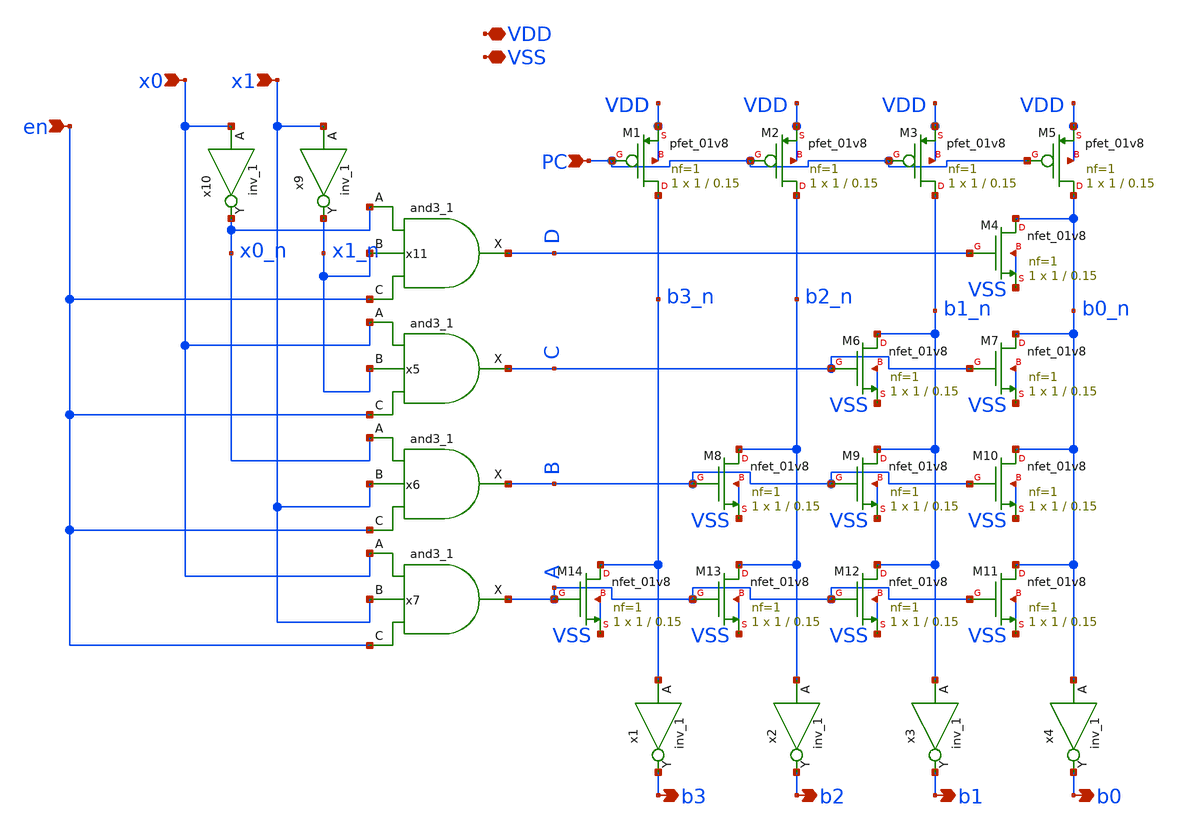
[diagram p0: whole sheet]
** sch_path: xschem/NOR_ROM_2bit.sch
**.subckt NOR_ROM_2bit VDD VSS x0 b3 x1 b2 b1 b0 PC en
*.iopin VDD
*.iopin VSS
*.ipin x0
*.opin b3
*.ipin x1
*.opin b2
*.opin b1
*.opin b0
*.ipin PC
*.ipin en
XM4 b0_n D VSS VSS sky130_fd_pr__nfet_01v8 L=0.15 W=1 nf=1 ad='int((nf+1)/2) * W/nf * 0.29' as='int((nf+2)/2) * W/nf * 0.29'
+ pd='2*int((nf+1)/2) * (W/nf + 0.29)' ps='2*int((nf+2)/2) * (W/nf + 0.29)' nrd='0.29 / W' nrs='0.29 / W'
+ sa=0 sb=0 sd=0 mult=1 m=1
XM6 b1_n C VSS VSS sky130_fd_pr__nfet_01v8 L=0.15 W=1 nf=1 ad='int((nf+1)/2) * W/nf * 0.29' as='int((nf+2)/2) * W/nf * 0.29'
+ pd='2*int((nf+1)/2) * (W/nf + 0.29)' ps='2*int((nf+2)/2) * (W/nf + 0.29)' nrd='0.29 / W' nrs='0.29 / W'
+ sa=0 sb=0 sd=0 mult=1 m=1
XM7 b0_n C VSS VSS sky130_fd_pr__nfet_01v8 L=0.15 W=1 nf=1 ad='int((nf+1)/2) * W/nf * 0.29' as='int((nf+2)/2) * W/nf * 0.29'
+ pd='2*int((nf+1)/2) * (W/nf + 0.29)' ps='2*int((nf+2)/2) * (W/nf + 0.29)' nrd='0.29 / W' nrs='0.29 / W'
+ sa=0 sb=0 sd=0 mult=1 m=1
XM8 b2_n B VSS VSS sky130_fd_pr__nfet_01v8 L=0.15 W=1 nf=1 ad='int((nf+1)/2) * W/nf * 0.29' as='int((nf+2)/2) * W/nf * 0.29'
+ pd='2*int((nf+1)/2) * (W/nf + 0.29)' ps='2*int((nf+2)/2) * (W/nf + 0.29)' nrd='0.29 / W' nrs='0.29 / W'
+ sa=0 sb=0 sd=0 mult=1 m=1
XM9 b1_n B VSS VSS sky130_fd_pr__nfet_01v8 L=0.15 W=1 nf=1 ad='int((nf+1)/2) * W/nf * 0.29' as='int((nf+2)/2) * W/nf * 0.29'
+ pd='2*int((nf+1)/2) * (W/nf + 0.29)' ps='2*int((nf+2)/2) * (W/nf + 0.29)' nrd='0.29 / W' nrs='0.29 / W'
+ sa=0 sb=0 sd=0 mult=1 m=1
XM10 b0_n B VSS VSS sky130_fd_pr__nfet_01v8 L=0.15 W=1 nf=1 ad='int((nf+1)/2) * W/nf * 0.29' as='int((nf+2)/2) * W/nf * 0.29'
+ pd='2*int((nf+1)/2) * (W/nf + 0.29)' ps='2*int((nf+2)/2) * (W/nf + 0.29)' nrd='0.29 / W' nrs='0.29 / W'
+ sa=0 sb=0 sd=0 mult=1 m=1
XM11 b0_n A VSS VSS sky130_fd_pr__nfet_01v8 L=0.15 W=1 nf=1 ad='int((nf+1)/2) * W/nf * 0.29' as='int((nf+2)/2) * W/nf * 0.29'
+ pd='2*int((nf+1)/2) * (W/nf + 0.29)' ps='2*int((nf+2)/2) * (W/nf + 0.29)' nrd='0.29 / W' nrs='0.29 / W'
+ sa=0 sb=0 sd=0 mult=1 m=1
XM12 b1_n A VSS VSS sky130_fd_pr__nfet_01v8 L=0.15 W=1 nf=1 ad='int((nf+1)/2) * W/nf * 0.29' as='int((nf+2)/2) * W/nf * 0.29'
+ pd='2*int((nf+1)/2) * (W/nf + 0.29)' ps='2*int((nf+2)/2) * (W/nf + 0.29)' nrd='0.29 / W' nrs='0.29 / W'
+ sa=0 sb=0 sd=0 mult=1 m=1
XM13 b2_n A VSS VSS sky130_fd_pr__nfet_01v8 L=0.15 W=1 nf=1 ad='int((nf+1)/2) * W/nf * 0.29' as='int((nf+2)/2) * W/nf * 0.29'
+ pd='2*int((nf+1)/2) * (W/nf + 0.29)' ps='2*int((nf+2)/2) * (W/nf + 0.29)' nrd='0.29 / W' nrs='0.29 / W'
+ sa=0 sb=0 sd=0 mult=1 m=1
XM14 b3_n A VSS VSS sky130_fd_pr__nfet_01v8 L=0.15 W=1 nf=1 ad='int((nf+1)/2) * W/nf * 0.29' as='int((nf+2)/2) * W/nf * 0.29'
+ pd='2*int((nf+1)/2) * (W/nf + 0.29)' ps='2*int((nf+2)/2) * (W/nf + 0.29)' nrd='0.29 / W' nrs='0.29 / W'
+ sa=0 sb=0 sd=0 mult=1 m=1
x1 b3_n VGND VNB VPB VPWR b3 sky130_fd_sc_hd__inv_1
x2 b2_n VGND VNB VPB VPWR b2 sky130_fd_sc_hd__inv_1
x3 b1_n VGND VNB VPB VPWR b1 sky130_fd_sc_hd__inv_1
x4 b0_n VGND VNB VPB VPWR b0 sky130_fd_sc_hd__inv_1
x9 x1 VGND VNB VPB VPWR x1_n sky130_fd_sc_hd__inv_1
x10 x0 VGND VNB VPB VPWR x0_n sky130_fd_sc_hd__inv_1
XM1 b3_n PC VDD VDD sky130_fd_pr__pfet_01v8 L=0.15 W=1 nf=1 ad='int((nf+1)/2) * W/nf * 0.29' as='int((nf+2)/2) * W/nf * 0.29'
+ pd='2*int((nf+1)/2) * (W/nf + 0.29)' ps='2*int((nf+2)/2) * (W/nf + 0.29)' nrd='0.29 / W' nrs='0.29 / W'
+ sa=0 sb=0 sd=0 mult=1 m=1
XM2 b2_n PC VDD VDD sky130_fd_pr__pfet_01v8 L=0.15 W=1 nf=1 ad='int((nf+1)/2) * W/nf * 0.29' as='int((nf+2)/2) * W/nf * 0.29'
+ pd='2*int((nf+1)/2) * (W/nf + 0.29)' ps='2*int((nf+2)/2) * (W/nf + 0.29)' nrd='0.29 / W' nrs='0.29 / W'
+ sa=0 sb=0 sd=0 mult=1 m=1
XM3 b1_n PC VDD VDD sky130_fd_pr__pfet_01v8 L=0.15 W=1 nf=1 ad='int((nf+1)/2) * W/nf * 0.29' as='int((nf+2)/2) * W/nf * 0.29'
+ pd='2*int((nf+1)/2) * (W/nf + 0.29)' ps='2*int((nf+2)/2) * (W/nf + 0.29)' nrd='0.29 / W' nrs='0.29 / W'
+ sa=0 sb=0 sd=0 mult=1 m=1
XM5 b0_n PC VDD VDD sky130_fd_pr__pfet_01v8 L=0.15 W=1 nf=1 ad='int((nf+1)/2) * W/nf * 0.29' as='int((nf+2)/2) * W/nf * 0.29'
+ pd='2*int((nf+1)/2) * (W/nf + 0.29)' ps='2*int((nf+2)/2) * (W/nf + 0.29)' nrd='0.29 / W' nrs='0.29 / W'
+ sa=0 sb=0 sd=0 mult=1 m=1
x11 x0_n x1_n en VGND VNB VPB VPWR D sky130_fd_sc_hd__and3_1
x5 x0 x1_n en VGND VNB VPB VPWR C sky130_fd_sc_hd__and3_1
x6 x0_n x1 en VGND VNB VPB VPWR B sky130_fd_sc_hd__and3_1
x7 x0 x1 en VGND VNB VPB VPWR A sky130_fd_sc_hd__and3_1
**.ends
.end
